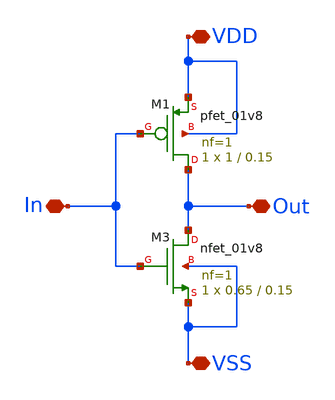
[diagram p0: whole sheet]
** sch_path: MUX/inverter_demux.sch
**.subckt inverter_demux VDD Out VSS In
*.iopin VDD
*.iopin Out
*.iopin VSS
*.iopin In
XM3 Out In VSS VSS sky130_fd_pr__nfet_01v8 L=0.15 W=0.65 nf=1 ad='int((nf+1)/2) * W/nf * 0.29' as='int((nf+2)/2) * W/nf * 0.29'
+ pd='2*int((nf+1)/2) * (W/nf + 0.29)' ps='2*int((nf+2)/2) * (W/nf + 0.29)' nrd='0.29 / W' nrs='0.29 / W'
+ sa=0 sb=0 sd=0 mult=1 m=1
XM1 Out In VDD VDD sky130_fd_pr__pfet_01v8 L=0.15 W=1 nf=1 ad='int((nf+1)/2) * W/nf * 0.29' as='int((nf+2)/2) * W/nf * 0.29'
+ pd='2*int((nf+1)/2) * (W/nf + 0.29)' ps='2*int((nf+2)/2) * (W/nf + 0.29)' nrd='0.29 / W' nrs='0.29 / W'
+ sa=0 sb=0 sd=0 mult=1 m=1
**.ends
.end
